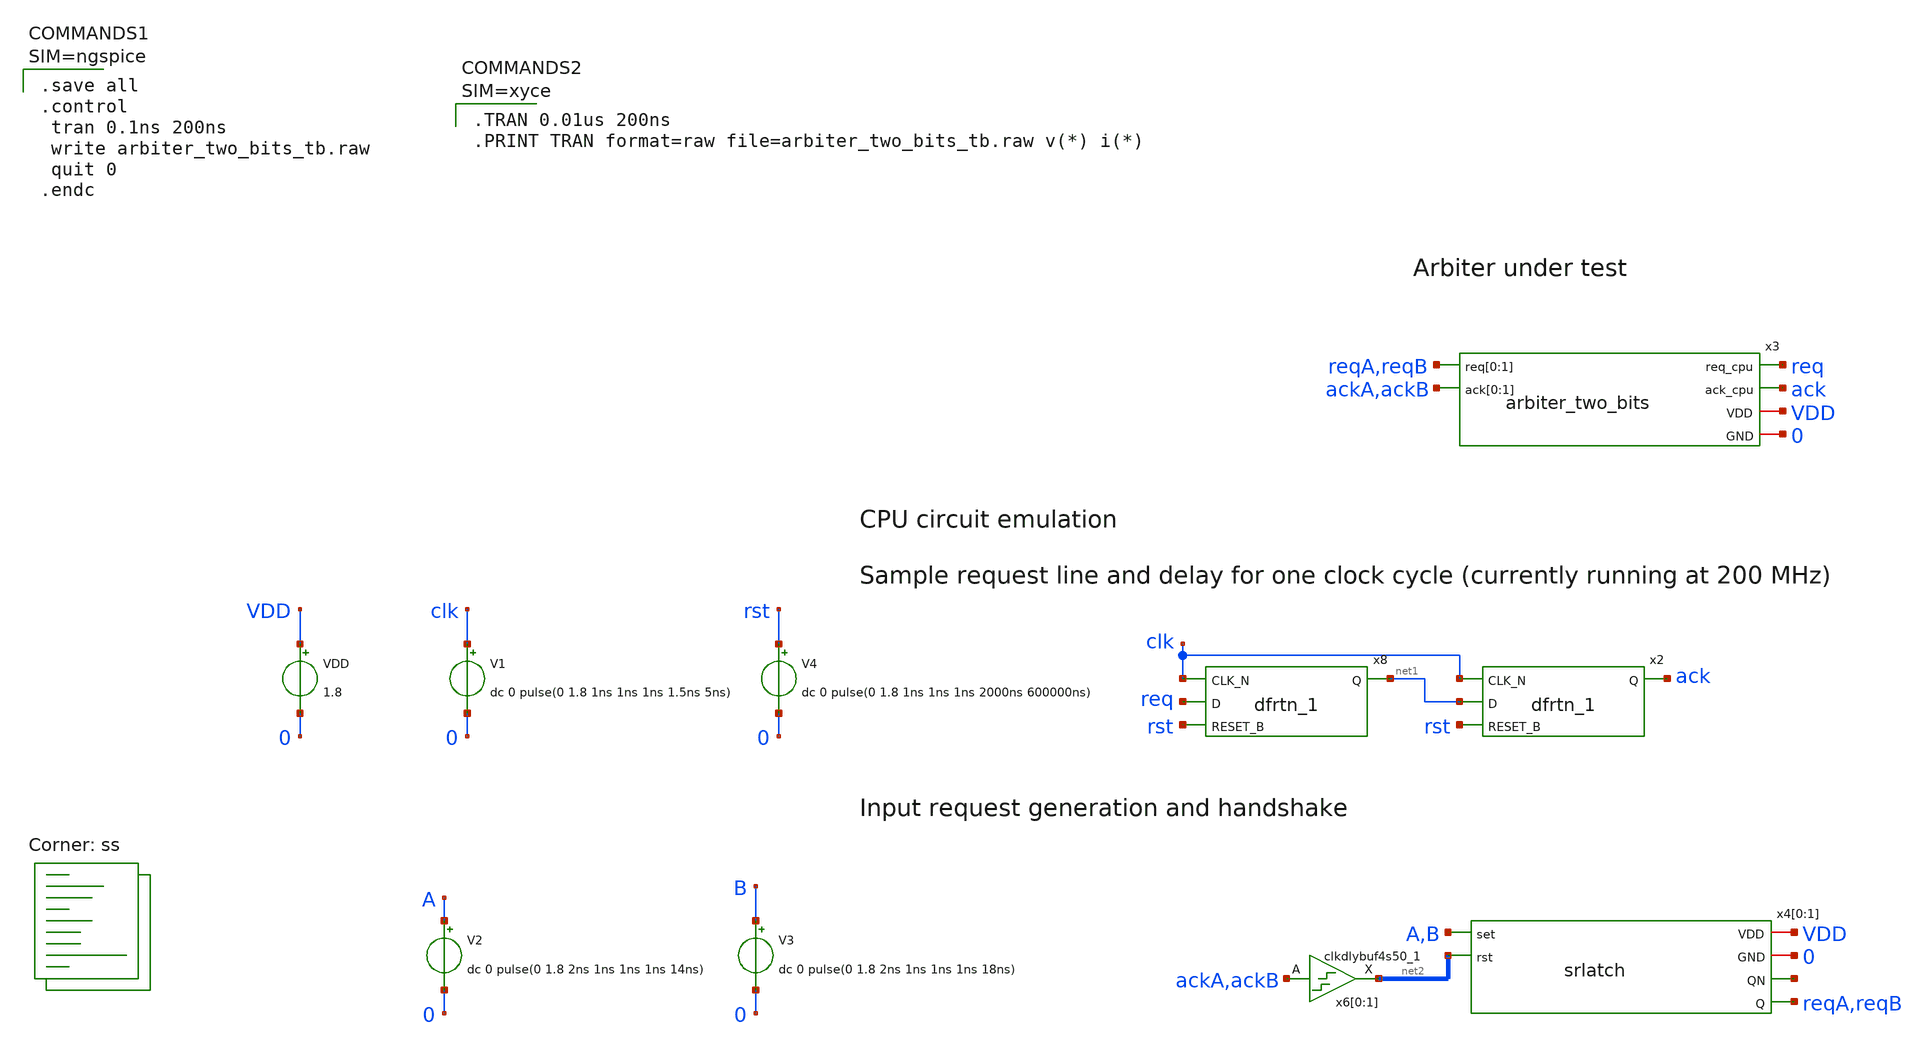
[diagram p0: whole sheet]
** sch_path: design/xschem/arbiter_two_bits_tb.sch
**.subckt arbiter_two_bits_tb
V3 B 0 dc 0 pulse(0 1.8 2ns 1ns 1ns 1ns 18ns)
V2 A 0 dc 0 pulse(0 1.8 2ns 1ns 1ns 1ns 14ns)
V1 clk 0 dc 0 pulse(0 1.8 1ns 1ns 1ns 1.5ns 5ns)
x4[0] VDD 0 A net3[1] reqA net2[1] srlatch
x4[1] VDD 0 B net3[0] reqB net2[0] srlatch
x6[0] ackA 0 0 VDD VDD net2[1] sky130_fd_sc_hd__clkdlybuf4s50_1
x6[1] ackB 0 0 VDD VDD net2[0] sky130_fd_sc_hd__clkdlybuf4s50_1
x8 clk req rst 0 0 VDD VDD net1 sky130_fd_sc_hd__dfrtn_1
x2 clk net1 rst 0 0 VDD VDD ack sky130_fd_sc_hd__dfrtn_1
V4 rst 0 dc 0 pulse(0 1.8 1ns 1ns 1ns 2000ns 600000ns)
x3 reqA reqB ack ackA ackB req VDD 0 arbiter_two_bits
VDD VDD 0 1.8
**** begin user architecture code
.lib $::SKYWATER_MODELS/sky130.lib.spice ss


* Standard cell simulation files
.include $::SKYWATER_STDCELLS/sky130_fd_sc_hd.spice







.save all
.control
 tran 0.1ns 200ns
 write arbiter_two_bits_tb.raw
 quit 0
.endc



**** end user architecture code
**.ends

* expanding   symbol:  srlatch.sym # of pins=6
** sym_path: design/xschem/srlatch.sym
** sch_path: design/xschem/srlatch.sch
.subckt srlatch VDD GND set QN Q rst
*.ipin set
*.ipin rst
*.opin Q
*.opin QN
*.iopin VDD
*.iopin GND
x1 set Q GND GND VDD VDD QN sky130_fd_sc_hd__nor2_1
x2 QN rst GND GND VDD VDD Q sky130_fd_sc_hd__nor2_1
.ends


* expanding   symbol:  arbiter_two_bits.sym # of pins=6
** sym_path: design/xschem/arbiter_two_bits.sym
** sch_path: design/xschem/arbiter_two_bits.sch
.subckt arbiter_two_bits req[0] req[1] ack_cpu ack[0] ack[1] req_cpu VDD GND
*.ipin req[0],req[1]
*.opin ack[0],ack[1]
*.ipin ack_cpu
*.opin req_cpu
*.iopin VDD
*.iopin GND
x1 ack[1] ack[0] ack_cpu req_cpu req[0] req[1] VDD GND arbiter_cell_two_bits_fc
.ends


* expanding   symbol:  arbiter_cell_two_bits_fc.sym # of pins=8
** sym_path: design/xschem/arbiter_cell_two_bits_fc.sym
** sch_path: design/xschem/arbiter_cell_two_bits_fc.sch
.subckt arbiter_cell_two_bits_fc g1 g0 gc rc r0 r1 VDD GND
*.ipin r1
*.ipin r0
*.opin g0
*.opin g1
*.opin rc
*.ipin gc
*.iopin GND
*.iopin VDD
x1 net6 net5 GND GND VDD VDD net7 sky130_fd_sc_hd__nand2_1
x2 r0 gc GND GND VDD VDD net4 sky130_fd_sc_hd__or2_1
x3 net3 net1 GND GND VDD VDD g0 sky130_fd_sc_hd__nor2_1
x4 net6 net6 net6 net6 GND GND VDD VDD net3 sky130_fd_sc_hd__or4_1
x5 gc GND GND VDD VDD net1 sky130_fd_sc_hd__inv_1
x6 gc r1 GND GND VDD VDD net5 sky130_fd_sc_hd__or2_1
x7 net4 net7 GND GND VDD VDD net6 sky130_fd_sc_hd__nand2_1
x8 net7 net7 net7 net7 GND GND VDD VDD net2 sky130_fd_sc_hd__or4_1
x9 net1 net2 GND GND VDD VDD g1 sky130_fd_sc_hd__nor2_1
x10 net2 r0 GND GND VDD VDD net8 sky130_fd_sc_hd__nand2_1
x11 net3 r1 GND GND VDD VDD net9 sky130_fd_sc_hd__nand2_1
x12 net8 net9 GND GND VDD VDD rc sky130_fd_sc_hd__nand2_1
.ends

.end
